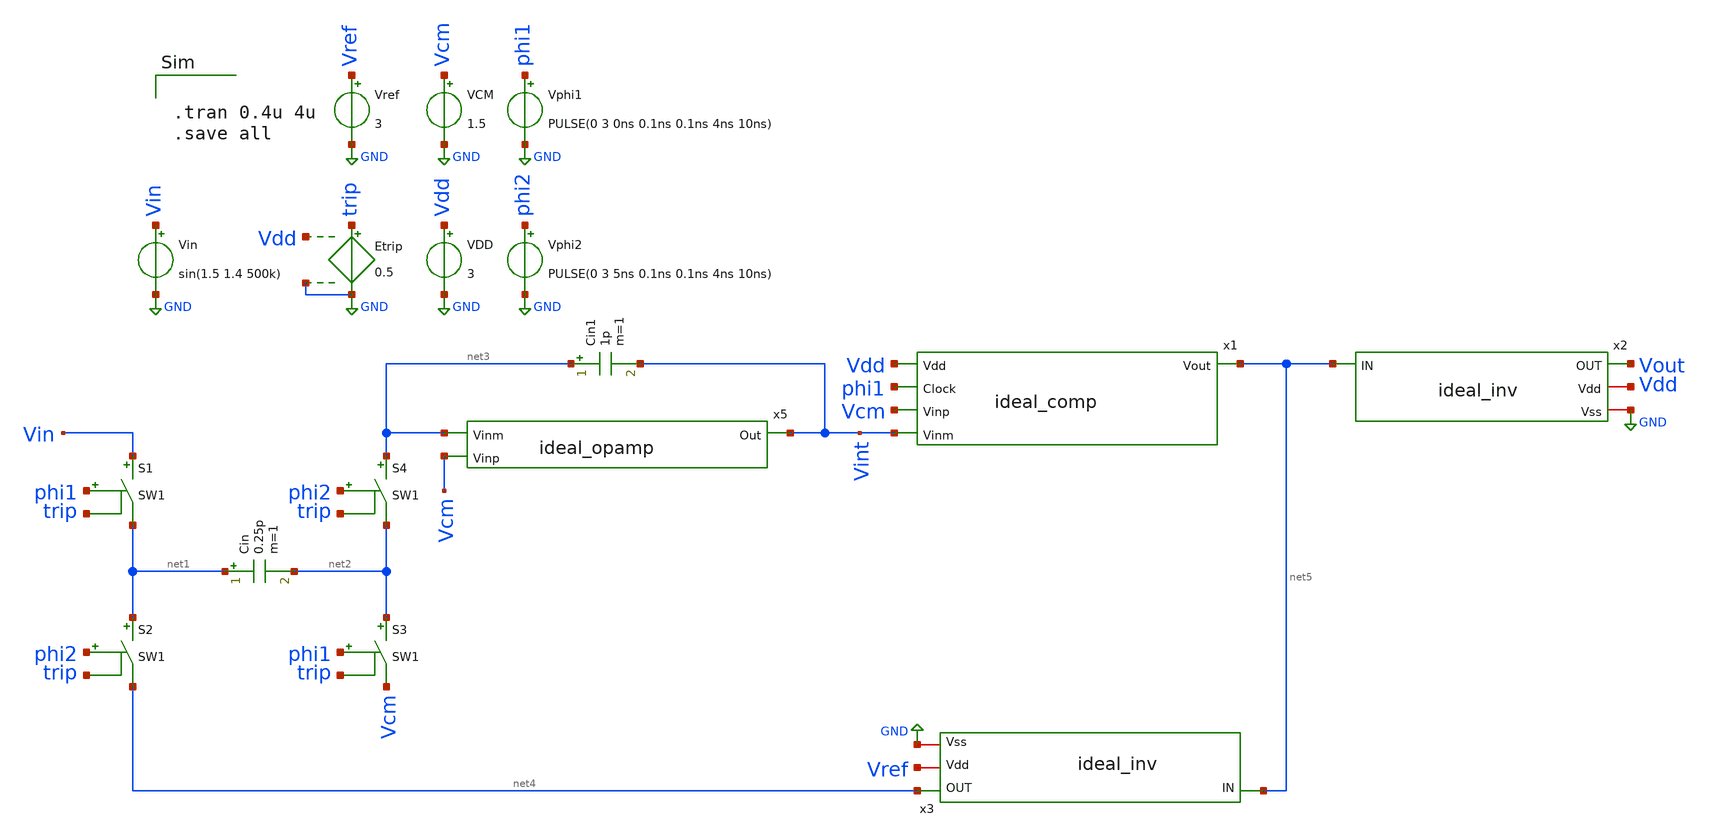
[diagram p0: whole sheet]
** sch_path: ideal_circuit/xschem/ideal_circuit.sch
**.subckt ideal_circuit
Etrip trip GND Vdd GND 0.5
Vref Vref GND 3
VDD Vdd GND 3
VCM Vcm GND 1.5
Vin Vin GND sin(1.5 1.4 500k)
Vphi1 phi1 GND PULSE(0 3 0ns 0.1ns 0.1ns 4ns 10ns)
Vphi2 phi2 GND PULSE(0 3 5ns 0.1ns 0.1ns 4ns 10ns)
Cin net1 net2 0.25p m=1
S2 net1 net4 phi2 trip SW1
S1 Vin net1 phi1 trip SW1
S3 net2 Vcm phi1 trip SW1
S4 net3 net2 phi2 trip SW1
Cin1 net3 Vint 1p m=1
x5 Vint net3 Vcm ideal_opamp
x1 net5 Vdd phi1 Vcm Vint ideal_comp
x3 net4 Vref net5 GND ideal_inv
x2 Vout Vdd net5 GND ideal_inv
**** begin user architecture code


.tran 0.4u 4u
.save all


**** end user architecture code
**.ends
.GLOBAL GND
**** begin user architecture code
.MODEL SW1 SW   VT=0.9 VH=0.01  RON=0.1 ROFF=10G
**** end user architecture code
.end
